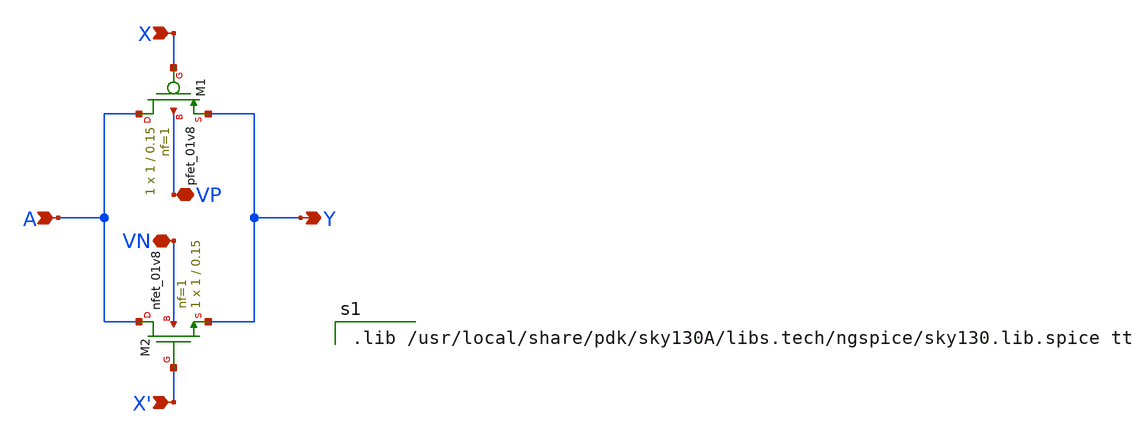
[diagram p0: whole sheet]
** sch_path: AllSymbols&Sch/GenericSym/TransmissionGate.sch
**.subckt TransmissionGate A Y X' X VP VN
*.ipin A
*.opin Y
*.ipin X'
*.ipin X
*.iopin VP
*.iopin VN
XM1 A X Y VP sky130_fd_pr__pfet_01v8 L=0.15 W=1 nf=1 ad='int((1 + 1)/2) * 1 / 1 * 0.29' as='int((1 + 2)/2) * 1 / 1 * 0.29'
+ pd='2*int((1 + 1)/2) * (1 / 1 + 0.29)' ps='2*int((1 + 2)/2) * (1 / 1 + 0.29)' nrd='0.29 / 1 ' nrs='0.29 / 1 '
+ sa=0 sb=0 sd=0 mult=1 m=1
XM2 A X' Y VN sky130_fd_pr__nfet_01v8 L=0.15 W=1 nf=1 ad='int((1 + 1)/2) * 1 / 1 * 0.29' as='int((1 +
+ 2)/2) * 1 / 1 * 0.29' pd='2*int((1 + 1)/2) * (1 / 1 + 0.29)' ps='2*int((1 + 2)/2) * (1 / 1 + 0.29)' nrd='0.29
+ / 1 ' nrs='0.29 / 1 ' sa=0 sb=0 sd=0 mult=1 m=1
**** begin user architecture code

.lib /usr/local/share/pdk/sky130A/libs.tech/ngspice/sky130.lib.spice tt

**** end user architecture code
**.ends
.end
